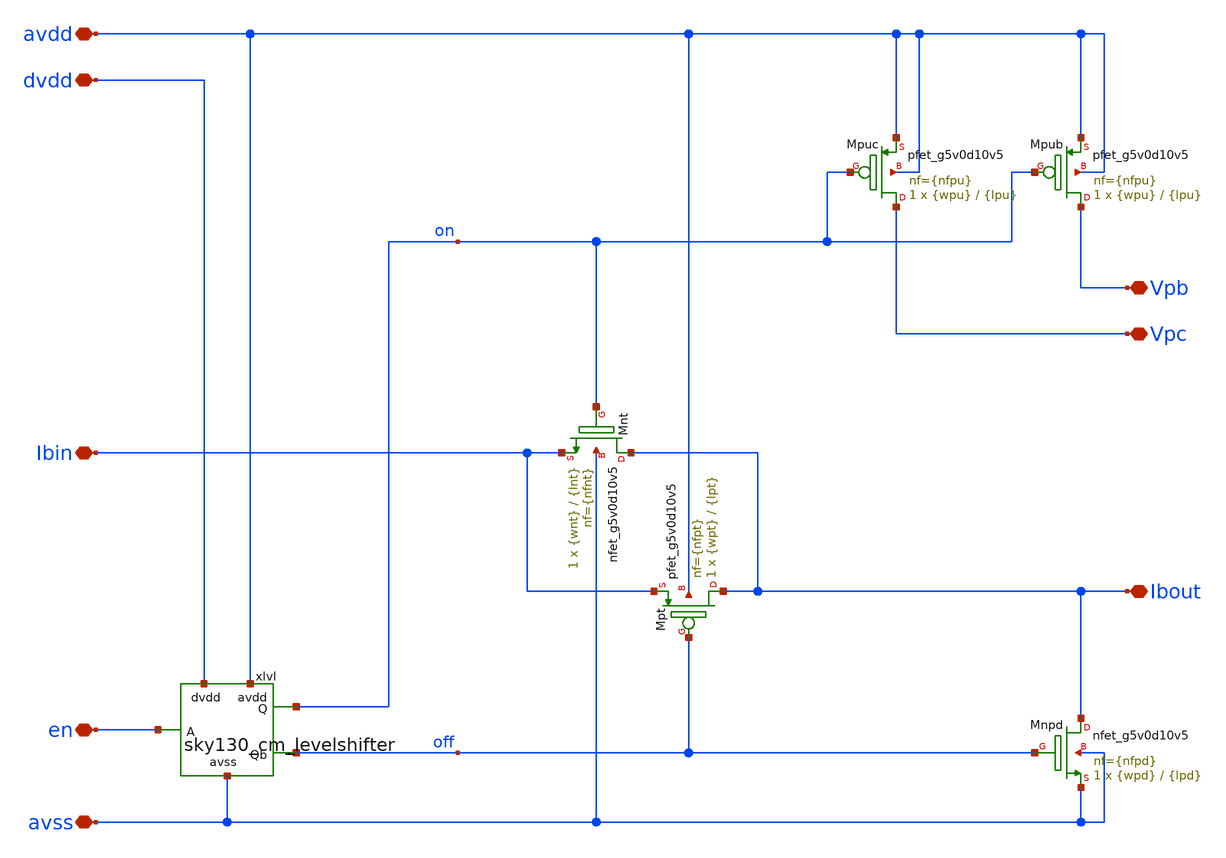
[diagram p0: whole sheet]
** sch_path: xschem/sky130_cm_poweroff.sch
**.subckt sky130_cm_poweroff avss avdd Ibin Vpb Vpc dvdd en Ibout
*.iopin avss
*.iopin avdd
*.iopin Ibin
*.iopin Vpb
*.iopin Vpc
*.iopin dvdd
*.iopin en
*.iopin Ibout
XMnpd Ibout off avss avss sky130_fd_pr__nfet_g5v0d10v5 L={lpd} W={wpd} nf={nfpd} ad='int(({nfpd} + 1)/2) * {wpd} / {nfpd} * 0.29'
+ as='int(({nfpd} + 2)/2) * {wpd} / {nfpd} * 0.29' pd='2*int(({nfpd} + 1)/2) * ({wpd} / {nfpd} + 0.29)'
+ ps='2*int(({nfpd} + 2)/2) * ({wpd} / {nfpd} + 0.29)' nrd='0.29 / {wpd} ' nrs='0.29 / {wpd} ' sa=0 sb=0
+ sd=0 mult=1 m=1
xlvl avdd on dvdd off en avss sky130_cm_levelshifter
XMpt Ibout off Ibin avdd sky130_fd_pr__pfet_g5v0d10v5 L={lpt} W={wpt} nf={nfpt} ad='int(({nfpt} + 1)/2) * {wpt} / {nfpt} * 0.29'
+ as='int(({nfpt} + 2)/2) * {wpt} / {nfpt} * 0.29' pd='2*int(({nfpt} + 1)/2) * ({wpt} / {nfpt} + 0.29)'
+ ps='2*int(({nfpt} + 2)/2) * ({wpt} / {nfpt} + 0.29)' nrd='0.29 / {wpt} ' nrs='0.29 / {wpt} ' sa=0 sb=0
+ sd=0 mult=1 m=1
XMnt Ibout on Ibin avss sky130_fd_pr__nfet_g5v0d10v5 L={lnt} W={wnt} nf={nfnt} ad='int(({nfnt} + 1)/2) * {wnt} / {nfnt} * 0.29'
+ as='int(({nfnt} + 2)/2) * {wnt} / {nfnt} * 0.29' pd='2*int(({nfnt} + 1)/2) * ({wnt} / {nfnt} + 0.29)'
+ ps='2*int(({nfnt} + 2)/2) * ({wnt} / {nfnt} + 0.29)' nrd='0.29 / {wnt} ' nrs='0.29 / {wnt} ' sa=0 sb=0
+ sd=0 mult=1 m=1
XMpuc Vpc on avdd avdd sky130_fd_pr__pfet_g5v0d10v5 L={lpu} W={wpu} nf={nfpu} ad='int(({nfpu} + 1)/2) * {wpu} / {nfpu} * 0.29'
+ as='int(({nfpu} + 2)/2) * {wpu} / {nfpu} * 0.29' pd='2*int(({nfpu} + 1)/2) * ({wpu} / {nfpu} + 0.29)'
+ ps='2*int(({nfpu} + 2)/2) * ({wpu} / {nfpu} + 0.29)' nrd='0.29 / {wpu} ' nrs='0.29 / {wpu} ' sa=0 sb=0
+ sd=0 mult=1 m=1
XMpub Vpb on avdd avdd sky130_fd_pr__pfet_g5v0d10v5 L={lpu} W={wpu} nf={nfpu} ad='int(({nfpu} + 1)/2) * {wpu} / {nfpu} * 0.29'
+ as='int(({nfpu} + 2)/2) * {wpu} / {nfpu} * 0.29' pd='2*int(({nfpu} + 1)/2) * ({wpu} / {nfpu} + 0.29)'
+ ps='2*int(({nfpu} + 2)/2) * ({wpu} / {nfpu} + 0.29)' nrd='0.29 / {wpu} ' nrs='0.29 / {wpu} ' sa=0 sb=0
+ sd=0 mult=1 m=1
**.ends

* expanding   symbol:  xschem/sky130_cm_levelshifter.sym # of pins=6
** sym_path: xschem/sky130_cm_levelshifter.sym
** sch_path: xschem/sky130_cm_levelshifter.sch
.subckt sky130_cm_levelshifter avdd Q dvdd Qb A avss
*.iopin avss
*.iopin avdd
*.iopin A
*.iopin dvdd
*.iopin Qb
*.iopin Q
XMnl1 Q ab avss avss sky130_fd_pr__nfet_g5v0d10v5 L=0.5 W=6 nf=1 ad='int((1 + 1)/2) * 6 / 1 * 0.29' as='int((1 + 2)/2) * 6 / 1 * 0.29'
+ pd='2*int((1 + 1)/2) * (6 / 1 + 0.29)' ps='2*int((1 + 2)/2) * (6 / 1 + 0.29)' nrd='0.29 / 6 ' nrs='0.29 / 6 '
+ sa=0 sb=0 sd=0 mult=1 m=1
XMnl2 Qb abb avss avss sky130_fd_pr__nfet_g5v0d10v5 L=0.5 W=6 nf=1 ad='int((1 + 1)/2) * 6 / 1 * 0.29'
+ as='int((1 + 2)/2) * 6 / 1 * 0.29' pd='2*int((1 + 1)/2) * (6 / 1 + 0.29)' ps='2*int((1 + 2)/2) * (6 / 1 + 0.29)'
+ nrd='0.29 / 6 ' nrs='0.29 / 6 ' sa=0 sb=0 sd=0 mult=1 m=1
XMpl1 Q Qb avdd avdd sky130_fd_pr__pfet_g5v0d10v5 L=0.5 W=2 nf=1 ad='int((1 + 1)/2) * 2 / 1 * 0.29' as='int((1 + 2)/2) * 2 / 1 * 0.29'
+ pd='2*int((1 + 1)/2) * (2 / 1 + 0.29)' ps='2*int((1 + 2)/2) * (2 / 1 + 0.29)' nrd='0.29 / 2 ' nrs='0.29 / 2 '
+ sa=0 sb=0 sd=0 mult=1 m=1
XMpl2 Qb Q avdd avdd sky130_fd_pr__pfet_g5v0d10v5 L=0.5 W=2 nf=1 ad='int((1 + 1)/2) * 2 / 1 * 0.29' as='int((1 + 2)/2) * 2 / 1 * 0.29'
+ pd='2*int((1 + 1)/2) * (2 / 1 + 0.29)' ps='2*int((1 + 2)/2) * (2 / 1 + 0.29)' nrd='0.29 / 2 ' nrs='0.29 / 2 '
+ sa=0 sb=0 sd=0 mult=1 m=1
XMn1 ab A avss avss sky130_fd_pr__nfet_01v8 L=0.15 W=1 nf=1 ad='int((1 + 1)/2) * 1 / 1 * 0.29' as='int((1 + 2)/2) * 1 / 1 * 0.29'
+ pd='2*int((1 + 1)/2) * (1 / 1 + 0.29)' ps='2*int((1 + 2)/2) * (1 / 1 + 0.29)' nrd='0.29 / 1 ' nrs='0.29 / 1 '
+ sa=0 sb=0 sd=0 mult=1 m=1
XMp1 ab A dvdd dvdd sky130_fd_pr__pfet_01v8 L=0.15 W=2 nf=1 ad='int((nf+1)/2) * W/nf * 0.29' as='int((nf+2)/2) * W/nf * 0.29'
+ pd='2*int((nf+1)/2) * (W/nf + 0.29)' ps='2*int((nf+2)/2) * (W/nf + 0.29)' nrd='0.29 / W' nrs='0.29 / W'
+ sa=0 sb=0 sd=0 mult=1 m=1
XMn2 abb ab avss avss sky130_fd_pr__nfet_01v8 L=0.15 W=1 nf=1 ad='int((1 + 1)/2) * 1 / 1 * 0.29' as='int((1 + 2)/2) * 1 / 1 * 0.29'
+ pd='2*int((1 + 1)/2) * (1 / 1 + 0.29)' ps='2*int((1 + 2)/2) * (1 / 1 + 0.29)' nrd='0.29 / 1 ' nrs='0.29 / 1 '
+ sa=0 sb=0 sd=0 mult=1 m=1
XMp2 abb ab dvdd dvdd sky130_fd_pr__pfet_01v8 L=0.15 W=2 nf=1 ad='int((nf+1)/2) * W/nf * 0.29' as='int((nf+2)/2) * W/nf * 0.29'
+ pd='2*int((nf+1)/2) * (W/nf + 0.29)' ps='2*int((nf+2)/2) * (W/nf + 0.29)' nrd='0.29 / W' nrs='0.29 / W'
+ sa=0 sb=0 sd=0 mult=1 m=1
.ends

.end
